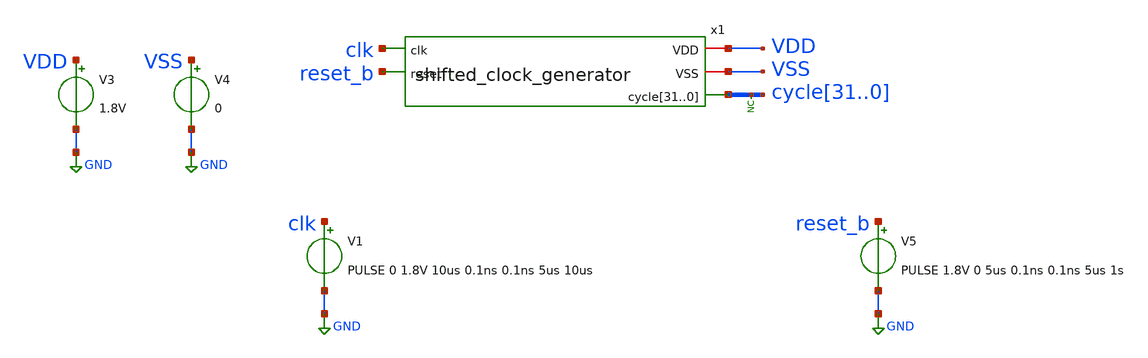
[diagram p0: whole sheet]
** sch_path: xschem/tests/shifted_clock_generator/shifted_clock_generator_test.sch
**.subckt shifted_clock_generator_test
V3 VDD GND 1.8V
V4 VSS GND 0
* noconn cycle[31..0]
V1 clk GND PULSE 0 1.8V 10us 0.1ns 0.1ns 5us 10us
V5 reset_b GND PULSE 1.8V 0 5us 0.1ns 0.1ns 5us 1s
x1 clk VDD VSS reset_b cycle31 cycle30 cycle29 cycle28 cycle27 cycle26 cycle25 cycle24 cycle23
+ cycle22 cycle21 cycle20 cycle19 cycle18 cycle17 cycle16 cycle15 cycle14 cycle13 cycle12 cycle11 cycle10
+ cycle9 cycle8 cycle7 cycle6 cycle5 cycle4 cycle3 cycle2 cycle1 cycle0 shifted_clock_generator
**** begin user architecture code
 .lib $::SKYWATER_MODELS/sky130.lib.spice tt
.include $::SKYWATER_STDCELLS/sky130_fd_sc_hd.spice


.options acct list
.temp 25
*vvcc VDD 0 dc 1.8
*vvss VSS 0 0
.control
tran 0.1u 400u
*plot RST_PLS clk+2 Pulse+4
plot reset_b-4 clk-2 cycle0 cycle1+2 cycle2+4 cycle3+6 cycle4+8 cycle5+10 cycle6+12 cycle7+14
+ cycle8+16 cycle9+18 cycle10+20 cycle11+22 cycle12+24 cycle13+26 cycle14+28 cycle15+30 cycle16+32 cycle17+34
+ cycle18+36 cycle19+38 cycle20+40 cycle21+42 cycle22+44  cycle23+46 cycle24+48 cycle25+50 cycle26+52 cycle27+54
+ cycle28+56 cycle29+58 cycle30+60 cycle31+62 x1.reset_cycle+64

write shifted_clock_generator_test.raw
.endc


**** end user architecture code
**.ends

* expanding   symbol:  src/shifted_clock_generator/shifted_clock_generator.sym # of pins=5
** sym_path: xschem/src/shifted_clock_generator/shifted_clock_generator.sym
** sch_path: xschem/src/shifted_clock_generator/shifted_clock_generator.sch
.subckt shifted_clock_generator clk VDD VSS reset cycle31 cycle30 cycle29 cycle28 cycle27 cycle26
+ cycle25 cycle24 cycle23 cycle22 cycle21 cycle20 cycle19 cycle18 cycle17 cycle16 cycle15 cycle14 cycle13
+ cycle12 cycle11 cycle10 cycle9 cycle8 cycle7 cycle6 cycle5 cycle4 cycle3 cycle2 cycle1 cycle0
*.opin
*+ cycle31,cycle30,cycle29,cycle28,cycle27,cycle26,cycle25,cycle24,cycle23,cycle22,cycle21,cycle20,cycle19,cycle18,cycle17,cycle16,cycle15,cycle14,cycle13,cycle12,cycle11,cycle10,cycle9,cycle8,cycle7,cycle6,cycle5,cycle4,cycle3,cycle2,cycle1,cycle0
*.iopin VSS
*.iopin VDD
*.ipin clk
*.ipin reset
x32 clk cycle0 reset_b VSS VSS VDD VDD cycle1 sky130_fd_sc_hd__dfrtp_1
x1 clk cycle1 reset_b VSS VSS VDD VDD cycle2 sky130_fd_sc_hd__dfrtp_1
x2 clk cycle2 reset_b VSS VSS VDD VDD cycle3 sky130_fd_sc_hd__dfrtp_1
x3 clk cycle3 reset_b VSS VSS VDD VDD cycle4 sky130_fd_sc_hd__dfrtp_1
x4 clk cycle4 reset_b VSS VSS VDD VDD cycle5 sky130_fd_sc_hd__dfrtp_1
x5 clk cycle5 reset_b VSS VSS VDD VDD cycle6 sky130_fd_sc_hd__dfrtp_1
x6 clk cycle6 reset_b VSS VSS VDD VDD cycle7 sky130_fd_sc_hd__dfrtp_1
x7 clk cycle7 reset_b VSS VSS VDD VDD cycle8 sky130_fd_sc_hd__dfrtp_1
x8 clk cycle8 reset_b VSS VSS VDD VDD cycle9 sky130_fd_sc_hd__dfrtp_1
x9 clk cycle9 reset_b VSS VSS VDD VDD cycle10 sky130_fd_sc_hd__dfrtp_1
x10 clk cycle10 reset_b VSS VSS VDD VDD cycle11 sky130_fd_sc_hd__dfrtp_1
x11 clk cycle11 reset_b VSS VSS VDD VDD cycle12 sky130_fd_sc_hd__dfrtp_1
x12 clk cycle12 reset_b VSS VSS VDD VDD cycle13 sky130_fd_sc_hd__dfrtp_1
x13 clk cycle13 reset_b VSS VSS VDD VDD cycle14 sky130_fd_sc_hd__dfrtp_1
x14 clk cycle14 reset_b VSS VSS VDD VDD cycle15 sky130_fd_sc_hd__dfrtp_1
x15 clk cycle15 reset_b VSS VSS VDD VDD cycle16 sky130_fd_sc_hd__dfrtp_1
x16 clk cycle16 reset_b VSS VSS VDD VDD cycle17 sky130_fd_sc_hd__dfrtp_1
x17 clk cycle17 reset_b VSS VSS VDD VDD cycle18 sky130_fd_sc_hd__dfrtp_1
x18 clk cycle18 reset_b VSS VSS VDD VDD cycle19 sky130_fd_sc_hd__dfrtp_1
x19 clk cycle19 reset_b VSS VSS VDD VDD cycle20 sky130_fd_sc_hd__dfrtp_1
x20 clk cycle20 reset_b VSS VSS VDD VDD cycle21 sky130_fd_sc_hd__dfrtp_1
x21 clk cycle21 reset_b VSS VSS VDD VDD cycle22 sky130_fd_sc_hd__dfrtp_1
x22 clk cycle22 reset_b VSS VSS VDD VDD cycle23 sky130_fd_sc_hd__dfrtp_1
x23 clk cycle23 reset_b VSS VSS VDD VDD cycle24 sky130_fd_sc_hd__dfrtp_1
x24 clk cycle24 reset_b VSS VSS VDD VDD cycle25 sky130_fd_sc_hd__dfrtp_1
x25 clk cycle25 reset_b VSS VSS VDD VDD cycle26 sky130_fd_sc_hd__dfrtp_1
x26 clk cycle26 reset_b VSS VSS VDD VDD cycle27 sky130_fd_sc_hd__dfrtp_1
x27 clk cycle27 reset_b VSS VSS VDD VDD cycle28 sky130_fd_sc_hd__dfrtp_1
x28 clk cycle28 reset_b VSS VSS VDD VDD cycle29 sky130_fd_sc_hd__dfrtp_1
x29 clk cycle29 reset_b VSS VSS VDD VDD cycle30 sky130_fd_sc_hd__dfrtp_1
x30 clk cycle30 reset_b VSS VSS VDD VDD cycle31 sky130_fd_sc_hd__dfrtp_1
x31 clk VDD reset_b VSS VSS VDD VDD cycle0 sky130_fd_sc_hd__dfrtp_1
x37 net1 VSS VSS VDD VDD reset_b sky130_fd_sc_hd__buf_16
x35 reset_cycle reset VSS VSS VDD VDD net1 sky130_fd_sc_hd__and2_4
x34 net5 VSS VSS VDD VDD net6 sky130_fd_sc_hd__clkdlybuf4s50_1
x39 half_cycle net12 VSS VSS VDD VDD reset_cycle sky130_fd_sc_hd__xnor2_1
x36 net4 VSS VSS VDD VDD net5 sky130_fd_sc_hd__clkdlybuf4s50_1
x40 net3 VSS VSS VDD VDD net4 sky130_fd_sc_hd__clkdlybuf4s50_1
x41 net2 VSS VSS VDD VDD net3 sky130_fd_sc_hd__clkdlybuf4s50_1
x42 half_cycle VSS VSS VDD VDD net2 sky130_fd_sc_hd__clkdlybuf4s50_1
x33 net7 cycle31 reset_b VSS VSS VDD VDD half_cycle sky130_fd_sc_hd__dfrtn_1
x38 net11 VSS VSS VDD VDD net12 sky130_fd_sc_hd__clkdlybuf4s50_1
x43 net10 VSS VSS VDD VDD net11 sky130_fd_sc_hd__clkdlybuf4s50_1
x44 net9 VSS VSS VDD VDD net10 sky130_fd_sc_hd__clkdlybuf4s50_1
x45 net8 VSS VSS VDD VDD net9 sky130_fd_sc_hd__clkdlybuf4s50_1
x46 net6 VSS VSS VDD VDD net8 sky130_fd_sc_hd__clkdlybuf4s50_1
x47 clk VSS VSS VDD VDD net7 sky130_fd_sc_hd__buf_1
.ends

.GLOBAL GND
.end
